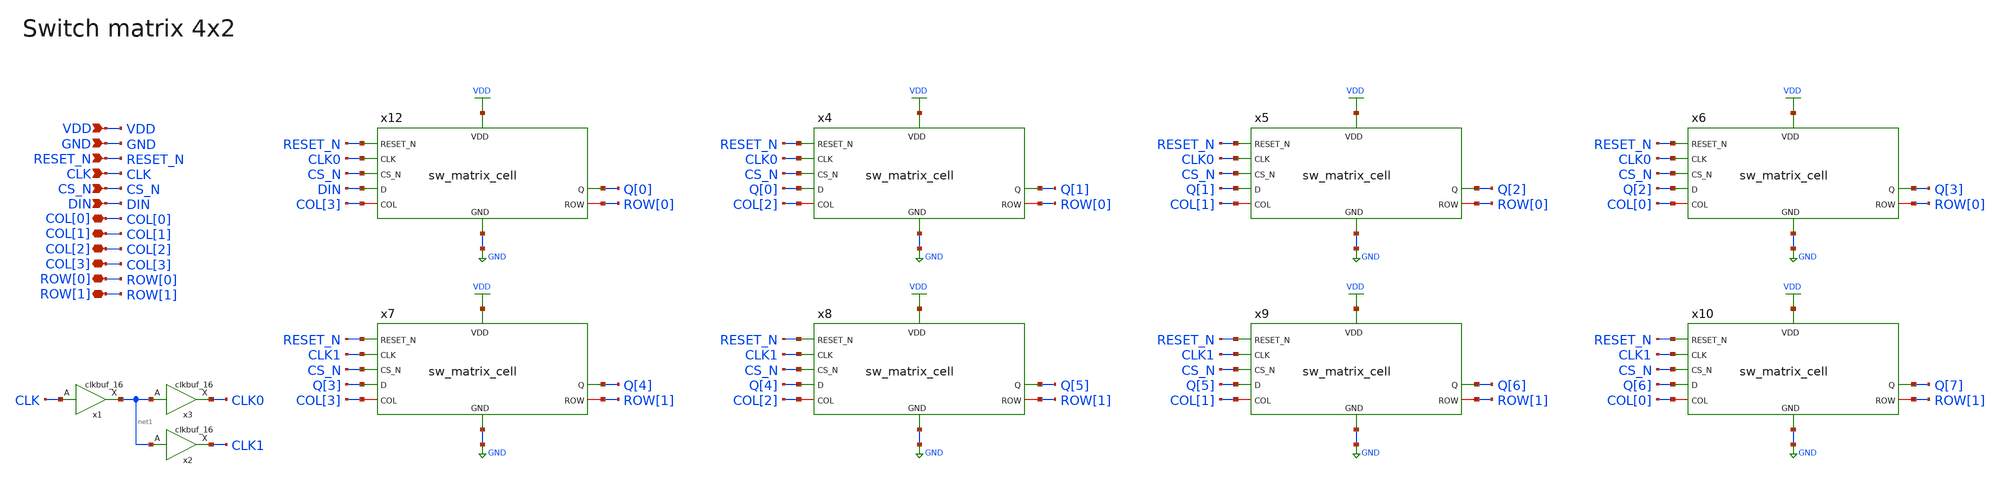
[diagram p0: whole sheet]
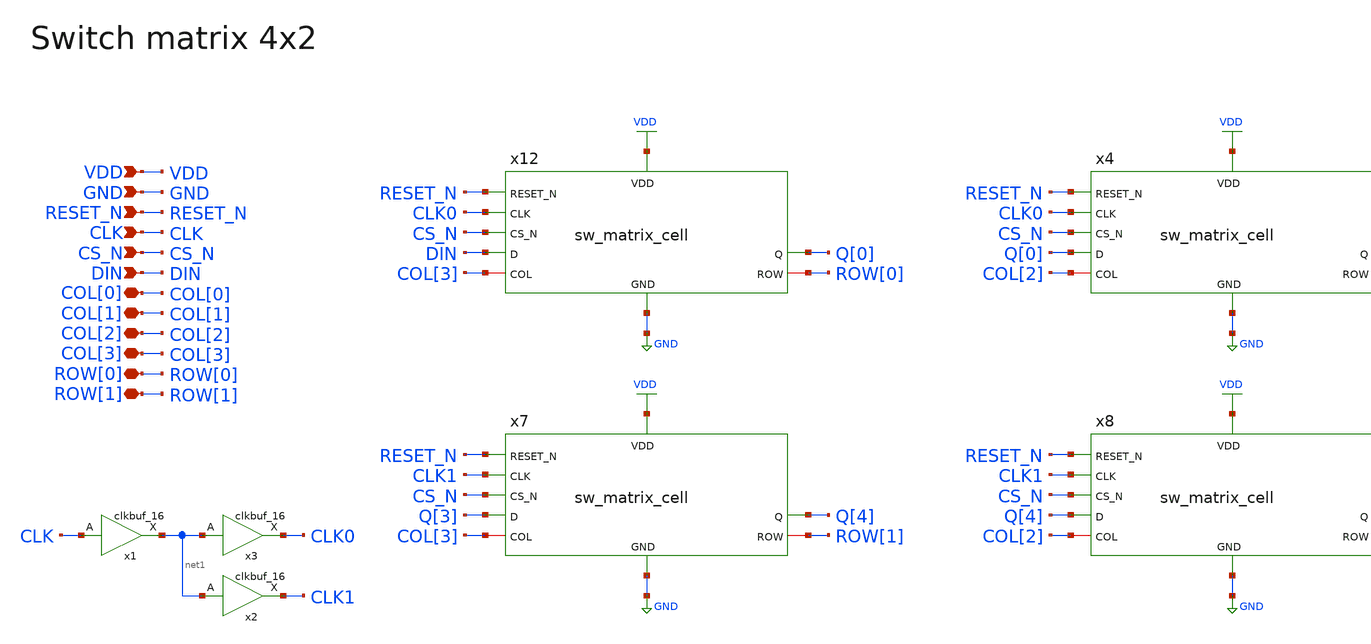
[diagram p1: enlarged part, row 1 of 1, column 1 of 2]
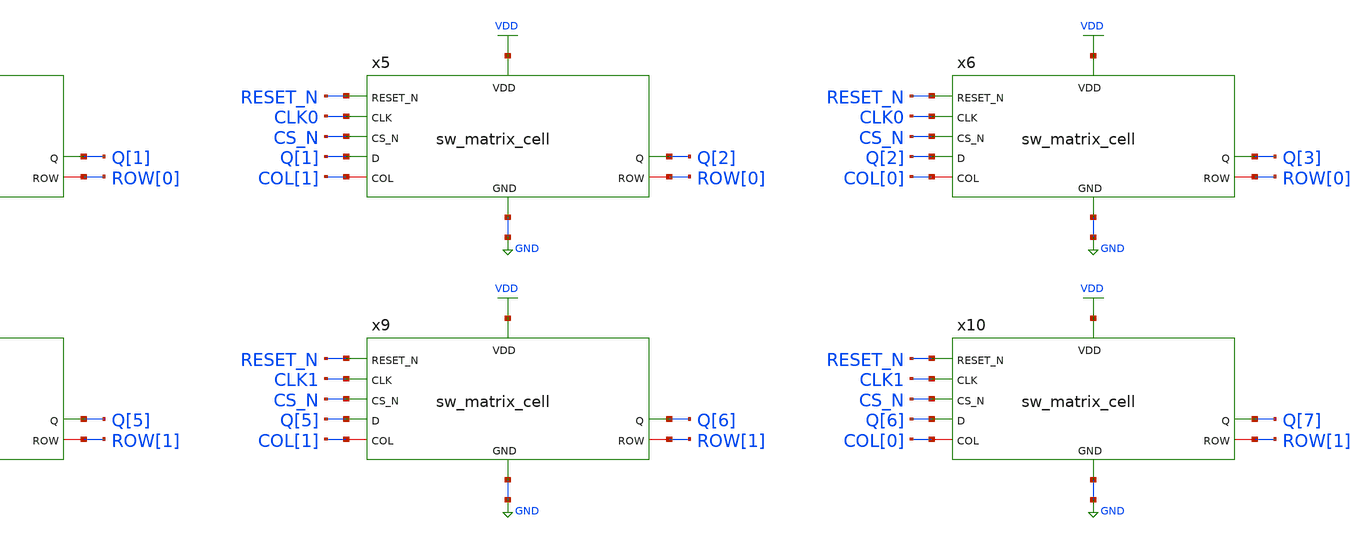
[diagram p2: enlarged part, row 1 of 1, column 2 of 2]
** sch_path: designs/libs/core_analog/sw_matrix/sw_matrix_4x2.sch
* Copyright 2022 GlobalFoundries PDK Authors
* Licensed under the Apache License, Version 2.0 (the "License");
* you may not use this file except in compliance with the License.
* You may obtain a copy of the License at
* https://www.apache.org/licenses/LICENSE-2.0
* Unless required by applicable law or agreed to in writing, software
* distributed under the License is distributed on an "AS IS" BASIS,
* WITHOUT WARRANTIES OR CONDITIONS OF ANY KIND, either express or implied.
* See the License for the specific language governing permissions and
* limitations under the License.
**.subckt sw_matrix_4x2 VDD GND RESET_N CLK CS_N DIN COL[0] COL[1] COL[2] COL[3] ROW[0] ROW[1]
*.ipin VDD
*.ipin GND
*.ipin RESET_N
*.ipin CLK
*.ipin CS_N
*.ipin DIN
*.iopin COL[0]
*.iopin COL[1]
*.iopin COL[2]
*.iopin COL[3]
*.iopin ROW[0]
*.iopin ROW[1]
x1 CLK net1 VPWR VNB VPB VGND gf180mcu_fd_sc_mcu7t5v0__clkbuf_16
x3 net1 CLK0 VPWR VNB VPB VGND gf180mcu_fd_sc_mcu7t5v0__clkbuf_16
x2 net1 CLK1 VPWR VNB VPB VGND gf180mcu_fd_sc_mcu7t5v0__clkbuf_16
x12 VDD GND RESET_N CLK0 DIN CS_N Q[0] COL[3] ROW[0] sw_matrix_cell
x4 VDD GND RESET_N CLK0 Q[0] CS_N Q[1] COL[2] ROW[0] sw_matrix_cell
x5 VDD GND RESET_N CLK0 Q[1] CS_N Q[2] COL[1] ROW[0] sw_matrix_cell
x6 VDD GND RESET_N CLK0 Q[2] CS_N Q[3] COL[0] ROW[0] sw_matrix_cell
x7 VDD GND RESET_N CLK1 Q[3] CS_N Q[4] COL[3] ROW[1] sw_matrix_cell
x8 VDD GND RESET_N CLK1 Q[4] CS_N Q[5] COL[2] ROW[1] sw_matrix_cell
x9 VDD GND RESET_N CLK1 Q[5] CS_N Q[6] COL[1] ROW[1] sw_matrix_cell
x10 VDD GND RESET_N CLK1 Q[6] CS_N Q[7] COL[0] ROW[1] sw_matrix_cell
**.ends
.GLOBAL GND
.GLOBAL VDD
.end
